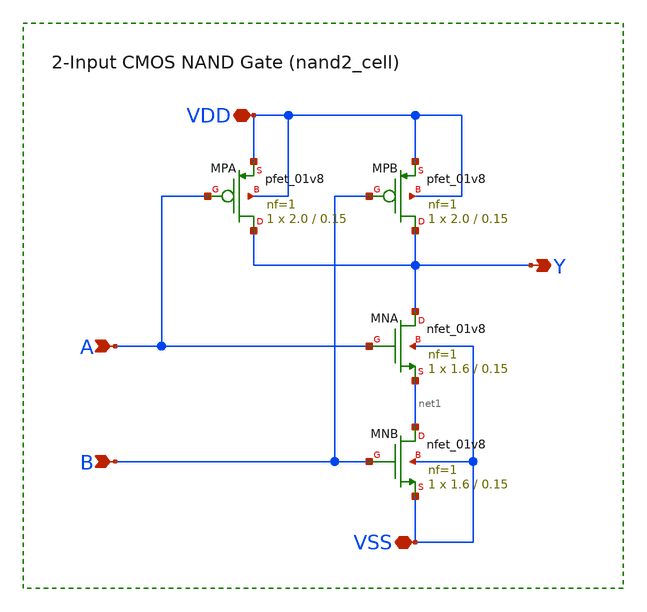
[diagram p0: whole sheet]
** sch_path: sky130-sc-lpf/xschem/nand2_cell.sch
**.subckt nand2_cell VDD Y VSS A B
*.iopin VDD
*.opin Y
*.iopin VSS
*.ipin A
*.ipin B
XMPA Y A VDD VDD sky130_fd_pr__pfet_01v8 L=0.15 W=2.0 nf=1 ad='int((nf+1)/2) * W/nf * 0.29' as='int((nf+2)/2) * W/nf * 0.29'
+ pd='2*int((nf+1)/2) * (W/nf + 0.29)' ps='2*int((nf+2)/2) * (W/nf + 0.29)' nrd='0.29 / W' nrs='0.29 / W'
+ sa=0 sb=0 sd=0 mult=1 m=1
XMPB Y B VDD VDD sky130_fd_pr__pfet_01v8 L=0.15 W=2.0 nf=1 ad='int((nf+1)/2) * W/nf * 0.29' as='int((nf+2)/2) * W/nf * 0.29'
+ pd='2*int((nf+1)/2) * (W/nf + 0.29)' ps='2*int((nf+2)/2) * (W/nf + 0.29)' nrd='0.29 / W' nrs='0.29 / W'
+ sa=0 sb=0 sd=0 mult=1 m=1
XMNA Y A net1 VSS sky130_fd_pr__nfet_01v8 L=0.15 W=1.6 nf=1 ad='int((1 + 1)/2) * 1.6 / 1 * 0.29' as='int((1 + 2)/2) * 1.6 / 1 * 0.29'
+ pd='2*int((1 + 1)/2) * (1.6 / 1 + 0.29)' ps='2*int((1 + 2)/2) * (1.6 / 1 + 0.29)' nrd='0.29 / 1.6 ' nrs='0.29 / 1.6 '
+ sa=0 sb=0 sd=0 mult=1 m=1
XMNB net1 B VSS VSS sky130_fd_pr__nfet_01v8 L=0.15 W=1.6 nf=1 ad='int((1 + 1)/2) * 1.6 / 1 * 0.29' as='int((1 + 2)/2) * 1.6 / 1 * 0.29'
+ pd='2*int((1 + 1)/2) * (1.6 / 1 + 0.29)' ps='2*int((1 + 2)/2) * (1.6 / 1 + 0.29)' nrd='0.29 / 1.6 ' nrs='0.29 / 1.6 '
+ sa=0 sb=0 sd=0 mult=1 m=1
**.ends
.end
